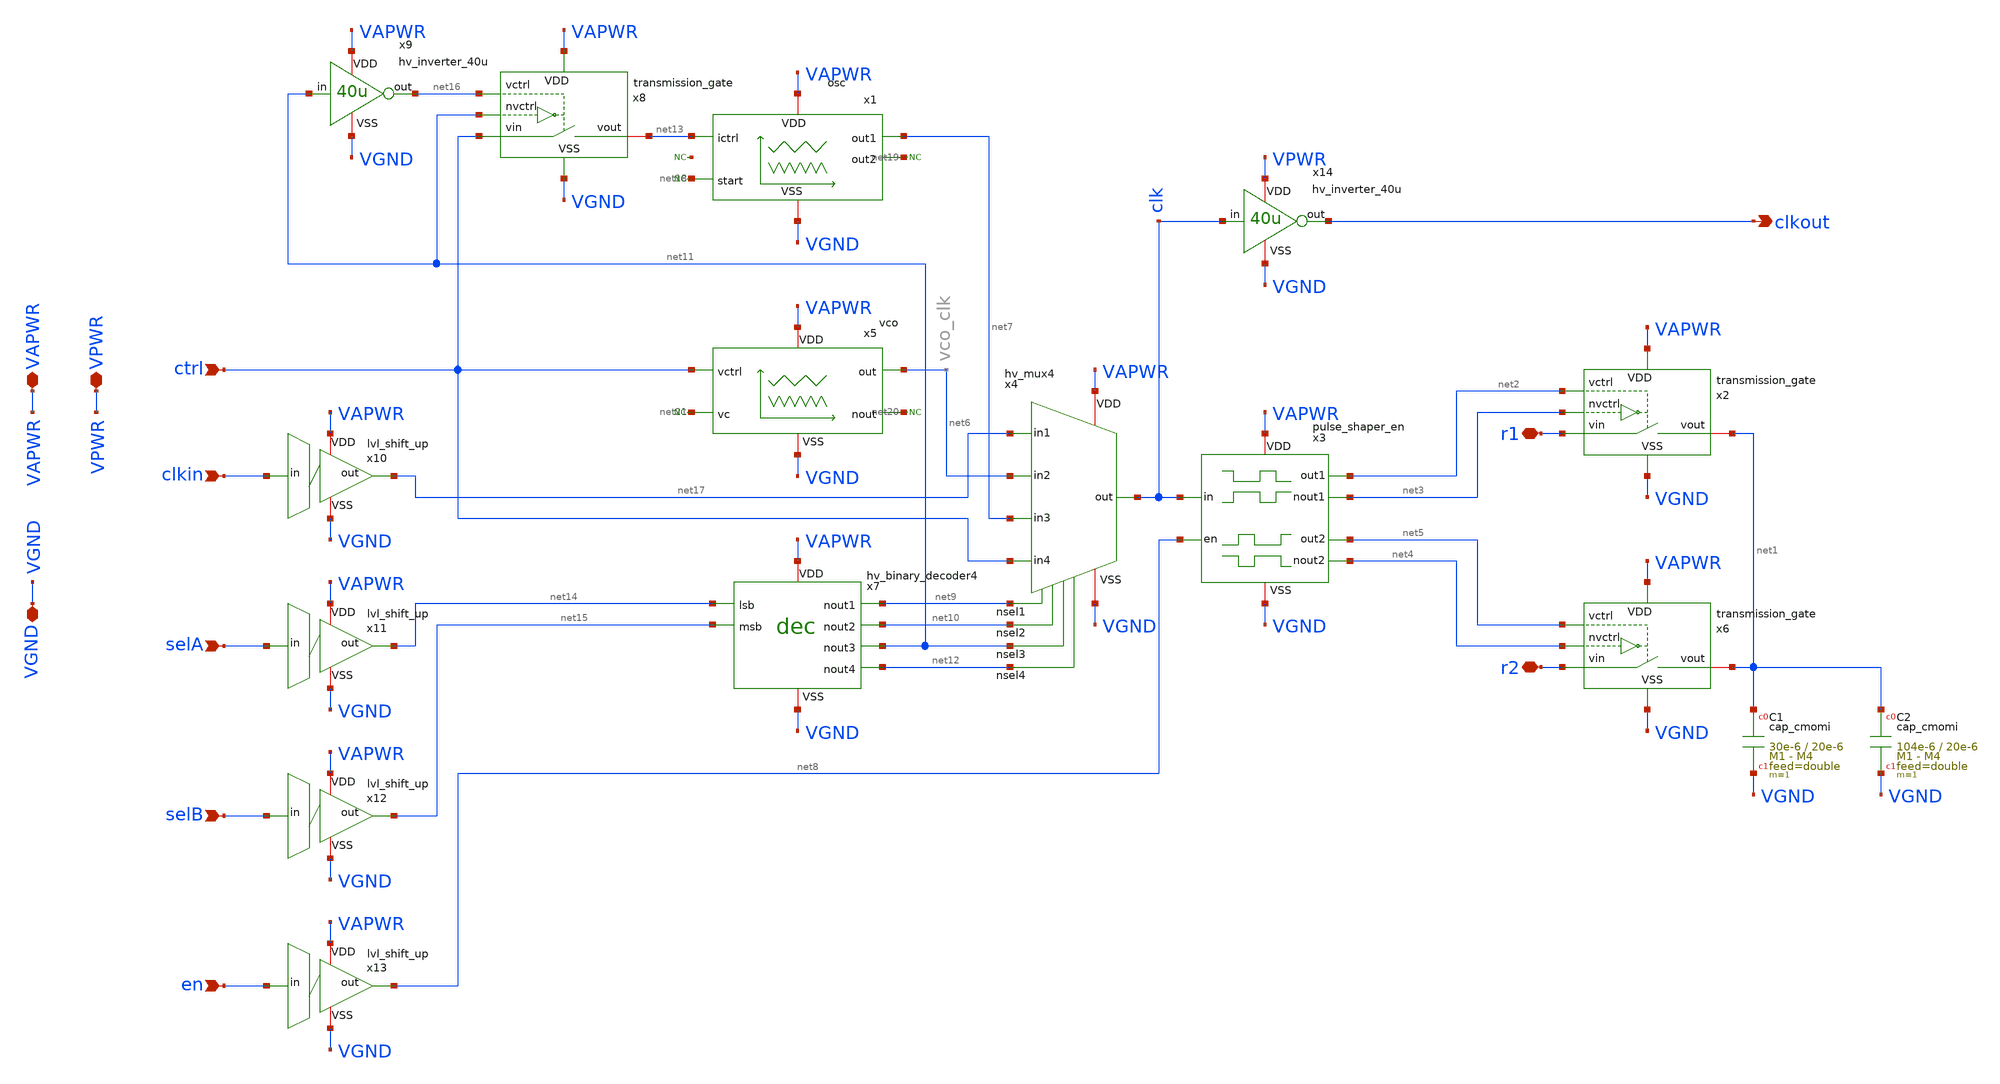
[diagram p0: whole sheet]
** sch_path: macros/heichips26_vcr/macros/switched_capacitor/schematic/xschem/switched_cap_cell.sch
**.subckt switched_cap_cell r1 r2 VAPWR VGND ctrl clkin selA selB en clkout VPWR
*.iopin r1
*.iopin r2
*.iopin VAPWR
*.iopin VGND
*.ipin ctrl
*.ipin clkin
*.ipin selA
*.ipin selB
*.ipin en
*.opin clkout
*.iopin VPWR
XC1 net1 VGND cap_cmomi w=30e-6 l=20e-6 mmin=1 mmax=4 feed=double subblock=0 m=1 mm_ok=1
x2 net2 r1 net1 net3 VAPWR VGND transmission_gate
x6 net5 r2 net1 net4 VAPWR VGND transmission_gate
x1 VAPWR net7 net13 VGND net18 net19 osc
x4 net9 VAPWR clk VGND net7 net17 ctrl net6 net10 net11 net12 hv_mux4
x5 VAPWR net6 VGND net20 ctrl net21 vco
x3 net2 net3 VAPWR clk VGND net5 net4 net8 pulse_shaper_en
x7 net15 net14 net9 net10 VAPWR VGND net11 net12 hv_binary_decoder4
* noconn #net21
* noconn #net22
* noconn #net18
* noconn #net19
* noconn #net20
x8 net16 ctrl net13 net11 VAPWR VGND transmission_gate
x9 VAPWR net11 net16 VGND hv_inverter_40u
XC2 net1 VGND cap_cmomi w=104e-6 l=20e-6 mmin=1 mmax=4 feed=double subblock=0 m=1 mm_ok=1
x10 VAPWR clkin net17 VGND lvl_shift_up
x11 VAPWR selA net14 VGND lvl_shift_up
x12 VAPWR selB net15 VGND lvl_shift_up
x13 VAPWR en net8 VGND lvl_shift_up
x14 VPWR clk clkout VGND hv_inverter_40u
**.ends

* expanding   symbol:  transmission_gate.sym # of pins=6
** sym_path: macros/heichips26_vcr/macros/switched_capacitor/schematic/xschem/transmission_gate.sym
** sch_path: macros/heichips26_vcr/macros/switched_capacitor/schematic/xschem/transmission_gate.sch
.subckt transmission_gate vctrl vin vout nvctrl VDD VSS
*.iopin vin
*.iopin vout
*.ipin vctrl
*.ipin nvctrl
*.iopin VDD
*.iopin VSS
XM3 vout vctrl vin VSS sg13_hv_nmos w={tg_ngate_w*tg_ng} l={tg_ch_len} ng={tg_ng} m=1 mm_ok=1
XM4 vout nvctrl vin VDD sg13_hv_pmos w={tg_pgate_w*tg_ng} l={tg_ch_len} ng={tg_ng} m=1 mm_ok=1
**** begin user architecture code


.param tg_ch_len=1u
.param tg_ngate_w=2u
.param tg_pgate_w=10u
.param tg_ng=20


**** end user architecture code
.ends


* expanding   symbol:  osc.sym # of pins=6
** sym_path: macros/heichips26_vcr/macros/switched_capacitor/schematic/xschem/osc.sym
** sch_path: macros/heichips26_vcr/macros/switched_capacitor/schematic/xschem/osc.sch
.subckt osc VDD out1 ictrl VSS start out2
*.iopin VSS
*.iopin VDD
*.iopin out2
*.iopin out1
*.iopin start
*.iopin ictrl
XM3 out1 ictrl VDD VDD sg13_hv_pmos w=10.0u l=2.0u ng=1 m=1 mm_ok=1
XM2 net1 ictrl VDD VDD sg13_hv_pmos w=1u l=2.0u ng=1 m=1 mm_ok=1
XM4 start ictrl VDD VDD sg13_hv_pmos w=1.0u l=2.0u ng=1 m=1 mm_ok=1
XM5 out2 ictrl VDD VDD sg13_hv_pmos w=10.0u l=2.0u ng=1 m=1 mm_ok=1
XM6 ictrl ictrl VDD VDD sg13_hv_pmos w=10.0u l=2.0u ng=1 m=1 mm_ok=1
XC1 net1 out1 cap_cmomi w=10e-6 l=10e-6 mmin=1 mmax=4 feed=double subblock=0 m=1 mm_ok=1
XC2 out2 start cap_cmomi w=10e-6 l=10e-6 mmin=1 mmax=4 feed=double subblock=0 m=1 mm_ok=1
XM8 out1 start VSS VSS sg13_hv_nmos w=3u l=0.45u ng=1 m=1 mm_ok=1
XM1 start start VSS VSS sg13_hv_nmos w=1u l=2u ng=1 m=1 mm_ok=1
XM12 out2 net1 VSS VSS sg13_hv_nmos w=3u l=0.45u ng=1 m=1 mm_ok=1
XM11 net1 net1 VSS VSS sg13_hv_nmos w=1u l=2u ng=1 m=1 mm_ok=1
**** begin user architecture code


.ic v(out1)=0 v(out2)=3.3


**** end user architecture code
.ends


* expanding   symbol:  hv_mux4.sym # of pins=11
** sym_path: macros/heichips26_vcr/macros/switched_capacitor/schematic/xschem/hv_mux4.sym
** sch_path: macros/heichips26_vcr/macros/switched_capacitor/schematic/xschem/hv_mux4.sch
.subckt hv_mux4 nsel1 VDD out VSS in3 in1 in4 in2 nsel2 nsel3 nsel4
*.ipin in1
*.iopin VDD
*.iopin VSS
*.opin out
*.ipin in2
*.ipin in3
*.ipin in4
*.ipin nsel1
*.ipin nsel3
*.ipin nsel2
*.ipin nsel4
x1 VDD net2 out net1 VSS net3 net4 hv_nor4
x2 VDD nsel1 net2 in1 VSS hv_nor
x4 VDD nsel2 net1 in2 VSS hv_nor
x5 VDD nsel3 net3 in3 VSS hv_nor
x6 VDD nsel4 net4 in4 VSS hv_nor
.ends


* expanding   symbol:  vco.sym # of pins=6
** sym_path: macros/heichips26_vcr/macros/switched_capacitor/schematic/xschem/vco.sym
** sch_path: macros/heichips26_vcr/macros/switched_capacitor/schematic/xschem/vco.sch
.subckt vco VDD out VSS nout vctrl vc
*.iopin VSS
*.iopin VDD
*.iopin nout
*.iopin out
*.iopin vctrl
*.iopin vc
**** begin user architecture code


.ic v(vc)=1.65


**** end user architecture code
XC1 vc VSS cap_cmomi w=30e-6 l=30e-6 mmin=1 mmax=4 feed=double subblock=0 m=1 mm_ok=1
XM4 vc out 5uA- VSS sg13_hv_nmos w=0.3u l=0.45u ng=1 m=1 mm_ok=1
x1 VDD s out nout r VSS hv_rs-ff
**** begin user architecture code


.param cm_n_w = 6u
.param cm_n_l = 5u
.param cm_p_w = 10u
.param cm_p_l = 2u

.param inv_ng = 1
.param inv_n_w = 2u
.param inv_n_l = 0.45u
.param inv_p_w = 6.5u
.param inv_p_l = 0.4u


**** end user architecture code
XM6 vc out 5uA+ VDD sg13_hv_pmos w=0.3u l=0.4u ng=1 m=1 mm_ok=1
x5 net2 vc vthl VDD 40uA- VSS comp_pmos
x7 net1 vthh vc VDD 40uA+ VSS comp_nmos
x2 10uA- vthl VDD vctrl VSS vthh voltage_mirror_pmos
x3 VDD net1 s VSS hv_inverter_6u5
x6 VDD net2 r VSS hv_inverter_6u5
x8 40uA+ 5uA+ VDD VSS 5uA- 10uA- 40uA- bias_current_generator
.ends


* expanding   symbol:  pulse_shaper_en.sym # of pins=8
** sym_path: macros/heichips26_vcr/macros/switched_capacitor/schematic/xschem/pulse_shaper_en.sym
** sch_path: macros/heichips26_vcr/macros/switched_capacitor/schematic/xschem/pulse_shaper_en.sch
.subckt pulse_shaper_en out1 nout1 VDD in VSS out2 nout2 en
*.opin out1
*.opin nout1
*.opin out2
*.opin nout2
*.ipin in
*.iopin VSS
*.iopin VDD
*.ipin en
x7 VDD net1 net3 VSS low_th_inverter
x8 VDD net1 net2 VSS high_th_inverter
x10 VDD out1 nout1 VSS hv_inverter_40u
x11 VDD nout2 out2 VSS hv_inverter_40u
**** begin user architecture code


.include ../../../netlist/pex/hv_inverter_0u3_magic_pex_3.spice
.param w   = 0.3u
.param ng  = 1
.param n_ng = ng
.param n_w = {w*n_ng}
.param n_l = 0.45u
.param p_ng = ng
.param p_w = {1*w*p_ng}
.param p_l = 0.4u


**** end user architecture code
x1 VDD in net1 VSS hv_inverter_0u3
x5 VDD net2 out1 net4 VSS hv_nor
x4 VDD net3 nout2 en VSS hv_nand
x3 VDD en net4 VSS hv_inverter_40u
.ends


* expanding   symbol:  hv_binary_decoder4.sym # of pins=8
** sym_path: macros/heichips26_vcr/macros/switched_capacitor/schematic/xschem/hv_binary_decoder4.sym
** sch_path: macros/heichips26_vcr/macros/switched_capacitor/schematic/xschem/hv_binary_decoder4.sch
.subckt hv_binary_decoder4 msb lsb nout1 nout2 VDD VSS nout3 nout4
*.iopin VDD
*.iopin VSS
*.ipin msb
*.ipin lsb
*.opin nout1
*.opin nout2
*.opin nout3
*.opin nout4
x3 VDD msb net1 VSS hv_inverter_40u
x7 VDD msb nout4 lsb VSS hv_nand
x9 VDD net1 nout2 lsb VSS hv_nand
x10 VDD lsb net2 VSS hv_inverter_40u
x11 VDD msb nout3 net2 VSS hv_nand
x8 VDD net1 nout1 net2 VSS hv_nand
.ends


* expanding   symbol:  hv_inverter_40u.sym # of pins=4
** sym_path: macros/heichips26_vcr/macros/switched_capacitor/schematic/xschem/hv_inverter_40u.sym
** sch_path: macros/heichips26_vcr/macros/switched_capacitor/schematic/xschem/hv_inverter_40u.sch
.subckt hv_inverter_40u VDD in out VSS
*.ipin in
*.iopin VDD
*.iopin VSS
*.opin out
XM2 out in VSS VSS sg13_hv_nmos w={n_w} l={n_l} ng={ng} m=1 mm_ok=1
XM3 out in VDD VDD sg13_hv_pmos w={p_w} l={p_l} ng={ng} m=1 mm_ok=1
**** begin user architecture code


.param w   = 10u
.param ng  = 4
.param n_ng = ng
.param n_w = {3u*n_ng}
.param n_l = 0.45u
.param p_ng = ng
.param p_w = {10u*p_ng}
.param p_l = 0.4u


**** end user architecture code
.ends


* expanding   symbol:  lvl_shift_up.sym # of pins=4
** sym_path: macros/heichips26_vcr/macros/switched_capacitor/schematic/xschem/lvl_shift_up.sym
** sch_path: macros/heichips26_vcr/macros/switched_capacitor/schematic/xschem/lvl_shift_up.sch
.subckt lvl_shift_up VDD in out VSS
*.ipin in
*.iopin VDD
*.iopin VSS
*.opin out
XM1 net1 in VSS VSS sg13_hv_nmos w={n_ng*n_w} l={n_l} ng={n_ng} m=1 mm_ok=1
XM2 net1 in VDD VDD sg13_hv_pmos w={p_ng*p_w} l={p_l} ng={n_ng} m=1 mm_ok=1
**** begin user architecture code


.param n_ng = 2
.param n_w = 10u
.param n_l = 0.45u
.param p_ng = 2
.param p_w = 1u
.param p_l = 0.45u


**** end user architecture code
x4 VDD net1 out VSS hv_inverter_6u5
.ends


* expanding   symbol:  hv_nor4.sym # of pins=7
** sym_path: macros/heichips26_vcr/macros/switched_capacitor/schematic/xschem/hv_nor4.sym
** sch_path: macros/heichips26_vcr/macros/switched_capacitor/schematic/xschem/hv_nor4.sch
.subckt hv_nor4 VDD in1 out in2 VSS in3 in4
*.ipin in1
*.iopin VDD
*.iopin VSS
*.opin out
*.ipin in2
*.ipin in3
*.ipin in4
**** begin user architecture code


.param w   = 10u
.param ng  = 4
.param n_ng = ng
.param n_w = {3u*n_ng}
.param n_l = 0.45u
.param p_ng = ng
.param p_w = {10u*p_ng}
.param p_l = 0.4u


**** end user architecture code
XM2 out in3 VSS VSS sg13_hv_nmos w={n_w} l={n_l} ng={ng} m=1 mm_ok=1
XM3 net3 in4 VDD VDD sg13_hv_pmos w={p_w} l={p_l} ng={ng} m=1 mm_ok=1
XM1 out in4 VSS VSS sg13_hv_nmos w={n_w} l={n_l} ng={ng} m=1 mm_ok=1
XM4 out in1 net1 VDD sg13_hv_pmos w={p_w} l={p_l} ng={ng} m=1 mm_ok=1
XM5 out in2 VSS VSS sg13_hv_nmos w={n_w} l={n_l} ng={ng} m=1 mm_ok=1
XM6 out in1 VSS VSS sg13_hv_nmos w={n_w} l={n_l} ng={ng} m=1 mm_ok=1
XM7 net1 in2 net2 VDD sg13_hv_pmos w={p_w} l={p_l} ng={ng} m=1 mm_ok=1
XM8 net2 in3 net3 VDD sg13_hv_pmos w={p_w} l={p_l} ng={ng} m=1 mm_ok=1
.ends


* expanding   symbol:  hv_nor.sym # of pins=5
** sym_path: macros/heichips26_vcr/macros/switched_capacitor/schematic/xschem/hv_nor.sym
** sch_path: macros/heichips26_vcr/macros/switched_capacitor/schematic/xschem/hv_nor.sch
.subckt hv_nor VDD in1 out in2 VSS
*.ipin in1
*.iopin VDD
*.iopin VSS
*.opin out
*.ipin in2
**** begin user architecture code


.param w   = 10u
.param ng  = 4
.param n_ng = ng
.param n_w = {3u*n_ng}
.param n_l = 0.45u
.param p_ng = ng
.param p_w = {10u*p_ng}
.param p_l = 0.4u


**** end user architecture code
XM2 out in1 VSS VSS sg13_hv_nmos w={n_w} l={n_l} ng={ng} m=1 mm_ok=1
XM3 net1 in2 VDD VDD sg13_hv_pmos w={p_w} l={p_l} ng={ng} m=1 mm_ok=1
XM1 out in2 VSS VSS sg13_hv_nmos w={n_w} l={n_l} ng={ng} m=1 mm_ok=1
XM4 out in1 net1 VDD sg13_hv_pmos w={p_w} l={p_l} ng={ng} m=1 mm_ok=1
.ends


* expanding   symbol:  hv_rs-ff.sym # of pins=6
** sym_path: macros/heichips26_vcr/macros/switched_capacitor/schematic/xschem/hv_rs-ff.sym
** sch_path: macros/heichips26_vcr/macros/switched_capacitor/schematic/xschem/hv_rs-ff.sch
.subckt hv_rs-ff VDD nS Q nQ nR VSS
*.ipin nS
*.iopin VDD
*.iopin VSS
*.opin Q
*.ipin nR
*.opin nQ
x4 VDD nS Q nQ VSS hv_nand
x5 VDD Q nQ nR VSS hv_nand
.ends


* expanding   symbol:  comp_pmos.sym # of pins=6
** sym_path: macros/heichips26_vcr/macros/switched_capacitor/schematic/xschem/comp_pmos.sym
** sch_path: macros/heichips26_vcr/macros/switched_capacitor/schematic/xschem/comp_pmos.sch
.subckt comp_pmos out - + VDD Ibias VSS
*.iopin VDD
*.iopin VSS
*.ipin Ibias
*.opin out
*.ipin +
*.ipin -
**** begin user architecture code


.param n_w = 1.2u
.param n_l = 1.5u
.param p_w = 2u
.param p_l = 0.4u
.param bcm = 1


**** end user architecture code
XM9 net1 Ibias VDD VDD sg13_hv_pmos w=bcm*p_w l=p_l ng=1 m=1 mm_ok=1
XM10 out Ibias VDD VDD sg13_hv_pmos w=bcm*p_w l=p_l ng=1 m=1 mm_ok=1
XM11 Ibias Ibias VDD VDD sg13_hv_pmos w=p_w l=p_l ng=1 m=1 mm_ok=1
XM12 net3 + net1 VDD sg13_hv_pmos w=p_w l=p_l ng=1 m=1 mm_ok=1
XM13 net2 - net1 VDD sg13_hv_pmos w=p_w l=p_l ng=1 m=1 mm_ok=1
XM14 net3 net2 VSS VSS sg13_hv_nmos w=n_w l=n_l ng=1 m=1 mm_ok=1
XM15 net2 net2 VSS VSS sg13_hv_nmos w=n_w l=n_l ng=1 m=1 mm_ok=1
XM16 out net3 VSS VSS sg13_hv_nmos w=n_w l=n_l ng=1 m=1 mm_ok=1
.ends


* expanding   symbol:  comp_nmos.sym # of pins=6
** sym_path: macros/heichips26_vcr/macros/switched_capacitor/schematic/xschem/comp_nmos.sym
** sch_path: macros/heichips26_vcr/macros/switched_capacitor/schematic/xschem/comp_nmos.sch
.subckt comp_nmos out - + VDD Ibias VSS
*.iopin VDD
*.iopin VSS
*.ipin -
*.ipin +
*.ipin Ibias
*.opin out
XM8 net2 + net3 VSS sg13_hv_nmos w=n_w l=n_l ng=1 m=1 mm_ok=1
XM6 net1 net1 VDD VDD sg13_hv_pmos w=p_w l=p_l ng=1 m=1 mm_ok=1
XM1 net2 net1 VDD VDD sg13_hv_pmos w=p_w l=p_l ng=1 m=1 mm_ok=1
XM3 net1 - net3 VSS sg13_hv_nmos w=n_w l=n_l ng=1 m=1 mm_ok=1
**** begin user architecture code


.param n_w = 1.2u
.param n_l = 1.5u
.param p_w = 2u
.param p_l = 0.4u


**** end user architecture code
XM2 out net2 VDD VDD sg13_hv_pmos w=p_w l=p_l ng=1 m=1 mm_ok=1
XM4 net3 Ibias VSS VSS sg13_hv_nmos w=2*n_w l=n_l ng=1 m=1 mm_ok=1
XM5 out Ibias VSS VSS sg13_hv_nmos w=2*n_w l=n_l ng=1 m=1 mm_ok=1
XM7 Ibias Ibias VSS VSS sg13_hv_nmos w=n_w l=n_l ng=1 m=1 mm_ok=1
.ends


* expanding   symbol:  voltage_mirror_pmos.sym # of pins=6
** sym_path: macros/heichips26_vcr/macros/switched_capacitor/schematic/xschem/voltage_mirror_pmos.sym
** sch_path: macros/heichips26_vcr/macros/switched_capacitor/schematic/xschem/voltage_mirror_pmos.sch
.subckt voltage_mirror_pmos Ibias nout VDD in VSS out
*.iopin VDD
*.iopin VSS
*.ipin in
*.opin out
*.opin nout
*.ipin Ibias
**** begin user architecture code


.param n_w = 6u
.param n_l = 5u
.param p_w = 10u
.param p_l = 2u


**** end user architecture code
XR1 in Ibias VSS rhigh w=0.5e-6 l=34e-6 m=1 b=0 mm_ok=1
XM4 net1 Ibias VDD VDD sg13_hv_pmos w=p_w l=p_l ng=1 m=1 mm_ok=1
XM5 out net1 VSS VSS sg13_hv_nmos w=n_w l=n_l ng=1 m=1 mm_ok=1
XR2 VSS nout VSS rhigh w=0.5e-6 l=34e-6 m=1 b=0 mm_ok=1
XR3 out VDD VSS rhigh w=0.5e-6 l=34e-6 m=1 b=0 mm_ok=1
XM2 net1 net1 VSS VSS sg13_hv_nmos w=n_w l=n_l ng=1 m=1 mm_ok=1
XM3 nout Ibias VDD VDD sg13_hv_pmos w=p_w l=p_l ng=1 m=1 mm_ok=1
XM6 Ibias Ibias VDD VDD sg13_hv_pmos w=1.9*p_w l=p_l ng=1 m=1 mm_ok=1
.ends


* expanding   symbol:  hv_inverter_6u5.sym # of pins=4
** sym_path: macros/heichips26_vcr/macros/switched_capacitor/schematic/xschem/hv_inverter_6u5.sym
** sch_path: macros/heichips26_vcr/macros/switched_capacitor/schematic/xschem/hv_inverter_6u5.sch
.subckt hv_inverter_6u5 VDD in out VSS
*.ipin in
*.iopin VDD
*.iopin VSS
*.opin out
XM2 out in VSS VSS sg13_hv_nmos w={n_w} l={n_l} ng={ng} m=1 mm_ok=1
XM3 out in VDD VDD sg13_hv_pmos w={p_w} l={p_l} ng={ng} m=1 mm_ok=1
**** begin user architecture code


.param ng  = 1
.param n_ng = ng
.param n_w = {2u*n_ng}
.param n_l = 0.45u
.param p_ng = ng
.param p_w = {6.5u*p_ng}
.param p_l = 0.4u


**** end user architecture code
.ends


* expanding   symbol:  bias_current_generator.sym # of pins=7
** sym_path: macros/heichips26_vcr/macros/switched_capacitor/schematic/xschem/bias_current_generator.sym
** sch_path: macros/heichips26_vcr/macros/switched_capacitor/schematic/xschem/bias_current_generator.sch
.subckt bias_current_generator 40uA+ 5uA+ VDD VSS 5uA- 10uA- 40uA-
*.opin 40uA+
*.iopin VSS
*.iopin VDD
*.opin 40uA-
*.opin 10uA-
*.opin 5uA+
*.opin 5uA-
x4 VDD net1 VSS current_reference_40uA
XM11 net1 net1 VDD VDD sg13_hv_pmos w=cm_p_w l=cm_p_l ng=1 m=1 mm_ok=1
XM12 40uA+ net1 VDD VDD sg13_hv_pmos w=cm_p_w l=cm_p_l ng=1 m=1 mm_ok=1
XM13 net2 net1 VDD VDD sg13_hv_pmos w=cm_p_w l=cm_p_l ng=1 m=1 mm_ok=1
XM14 net2 net2 VSS VSS sg13_hv_nmos w=cm_n_w l=cm_n_l ng=1 m=1 mm_ok=1
XM15 40uA- net2 VSS VSS sg13_hv_nmos w=cm_n_w l=cm_n_l ng=1 m=1 mm_ok=1
XM1 net3 net1 VDD VDD sg13_hv_pmos w=cm_p_w l=cm_p_l ng=1 m=1 mm_ok=1
XM2 net3 net3 VSS VSS sg13_hv_nmos w=4*cm_n_w l=cm_n_l ng=4 m=1 mm_ok=1
XM3 10uA- net3 VSS VSS sg13_hv_nmos w=cm_n_w l=cm_n_l ng=1 m=1 mm_ok=1
XM5 net4 net3 VSS VSS sg13_hv_nmos w=cm_n_w l=cm_n_l ng=1 m=1 mm_ok=1
XM25 net4 net4 VDD VDD sg13_hv_pmos w=2*cm_p_w l=cm_p_l ng=2 m=1 mm_ok=1
XM26 net5 net4 VDD VDD sg13_hv_pmos w=cm_p_w l=cm_p_l ng=1 m=1 mm_ok=1
XM27 5uA+ net4 VDD VDD sg13_hv_pmos w=cm_p_w l=cm_p_l ng=1 m=1 mm_ok=1
XM28 net5 net5 VSS VSS sg13_hv_nmos w=cm_n_w l=cm_n_l ng=2 m=1 mm_ok=1
XM29 5uA- net5 VSS VSS sg13_hv_nmos w=cm_n_w l=cm_n_l ng=1 m=1 mm_ok=1
**** begin user architecture code


.param cm_n_w = 6u
.param cm_n_l = 5u
.param cm_p_w = 10u
.param cm_p_l = 2u


**** end user architecture code
.ends


* expanding   symbol:  low_th_inverter.sym # of pins=4
** sym_path: macros/heichips26_vcr/macros/switched_capacitor/schematic/xschem/low_th_inverter.sym
** sch_path: macros/heichips26_vcr/macros/switched_capacitor/schematic/xschem/low_th_inverter.sch
.subckt low_th_inverter VDD vin vout VSS
*.ipin vin
*.iopin VDD
*.iopin VSS
*.opin vout
XM1 vout vin VSS VSS sg13_hv_nmos w={n_ng*n_w} l={n_l} ng={n_ng} m=1 mm_ok=1
XM2 vout vin VDD VDD sg13_hv_pmos w={p_ng*p_w} l={p_l} ng={n_ng} m=1 mm_ok=1
**** begin user architecture code


.param n_ng = 2
.param n_w = 1u
.param n_l = 0.45u
.param p_ng = 2
.param p_w = 1u
.param p_l = 0.4u


**** end user architecture code
.ends


* expanding   symbol:  high_th_inverter.sym # of pins=4
** sym_path: macros/heichips26_vcr/macros/switched_capacitor/schematic/xschem/high_th_inverter.sym
** sch_path: macros/heichips26_vcr/macros/switched_capacitor/schematic/xschem/high_th_inverter.sch
.subckt high_th_inverter VDD vin vout VSS
*.ipin vin
*.iopin VDD
*.iopin VSS
*.opin vout
XMdummy1 VSS VSS VSS VSS sg13_hv_nmos w=0.6u l=1.0u ng=2 m=1 mm_ok=1
XMdummy2 VDD VDD VDD VDD sg13_hv_pmos w=12.0u l=1.0u ng=2 m=1 mm_ok=1
XM1 vout vin VSS VSS sg13_hv_nmos w=6.0u l=1.0u ng=20 m=1 mm_ok=1
XM2 vout vin VDD VDD sg13_hv_pmos w=120.0u l=1.0u ng=20 m=1 mm_ok=1
.ends


* expanding   symbol:  hv_inverter_0u3.sym # of pins=4
** sym_path: macros/heichips26_vcr/macros/switched_capacitor/schematic/xschem/hv_inverter_0u3.sym
** sch_path: macros/heichips26_vcr/macros/switched_capacitor/schematic/xschem/hv_inverter_0u3.sch
.subckt hv_inverter_0u3 VDD in out VSS
*.ipin in
*.iopin VDD
*.iopin VSS
*.opin out
XM2 out in VSS VSS sg13_hv_nmos w={n_w} l={n_l} ng={ng} m=1 mm_ok=1
XM3 out in VDD VDD sg13_hv_pmos w={p_w} l={p_l} ng={ng} m=1 mm_ok=1
**** begin user architecture code


.param w   = 0.3u
.param ng  = 1
.param n_ng = ng
.param n_w = {w*n_ng}
.param n_l = 0.45u
.param p_ng = ng
.param p_w = {1*w*p_ng}
.param p_l = 0.4u


**** end user architecture code
.ends


* expanding   symbol:  hv_nand.sym # of pins=5
** sym_path: macros/heichips26_vcr/macros/switched_capacitor/schematic/xschem/hv_nand.sym
** sch_path: macros/heichips26_vcr/macros/switched_capacitor/schematic/xschem/hv_nand.sch
.subckt hv_nand VDD in1 out in2 VSS
*.ipin in1
*.iopin VDD
*.iopin VSS
*.opin out
*.ipin in2
**** begin user architecture code


.param w   = 10u
.param ng  = 4
.param n_ng = ng
.param n_w = {3u*n_ng}
.param n_l = 0.45u
.param p_ng = ng
.param p_w = {10u*p_ng}
.param p_l = 0.4u


**** end user architecture code
XM2 out in1 net1 VSS sg13_hv_nmos w={n_w} l={n_l} ng={ng} m=1 mm_ok=1
XM3 out in2 VDD VDD sg13_hv_pmos w={p_w} l={p_l} ng={ng} m=1 mm_ok=1
XM1 net1 in2 VSS VSS sg13_hv_nmos w={n_w} l={n_l} ng={ng} m=1 mm_ok=1
XM4 out in1 VDD VDD sg13_hv_pmos w={p_w} l={p_l} ng={ng} m=1 mm_ok=1
.ends


* expanding   symbol:  current_reference_40uA.sym # of pins=3
** sym_path: macros/heichips26_vcr/macros/switched_capacitor/schematic/xschem/current_reference_40uA.sym
** sch_path: macros/heichips26_vcr/macros/switched_capacitor/schematic/xschem/current_reference_40uA.sch
.subckt current_reference_40uA VDD iout VSS
*.iopin VSS
*.iopin VDD
*.iopin iout
XM8 net2 net2 VSS VSS sg13_hv_nmos w=n_w l=n_l ng=1 m=1 mm_ok=1
XM6 net2 net1 VDD VDD sg13_hv_pmos w=p_w l=p_l ng=1 m=1 mm_ok=1
XM1 net1 net1 VDD VDD sg13_hv_pmos w=p_w l=p_l ng=1 m=1 mm_ok=1
XM3 net1 net2 net3 VSS sg13_hv_nmos w=n_w l=n_l ng=1 m=1 mm_ok=1
XR2 net4 VSS VSS rppd w=2e-6 l=21.9e-6 m=1 b=0 mm_ok=1
XM2 net1 net2 net3 VSS sg13_hv_nmos w=n_w l=n_l ng=1 m=1 mm_ok=1
XM4 net1 net2 net3 VSS sg13_hv_nmos w=n_w l=n_l ng=1 m=1 mm_ok=1
XM5 net1 net2 net3 VSS sg13_hv_nmos w=n_w l=n_l ng=1 m=1 mm_ok=1
XM7 iout net2 VSS VSS sg13_hv_nmos w=n_w l=n_l ng=1 m=1 mm_ok=1
XR3 net3 net4 VSS rsil w=0.5e-6 l=365e-6 m=1 mm_ok=1
**** begin user architecture code


.param n_w = 6u
.param n_l = 5u
.param p_w = 10u
.param p_l = 2u


**** end user architecture code
.ends

.end
